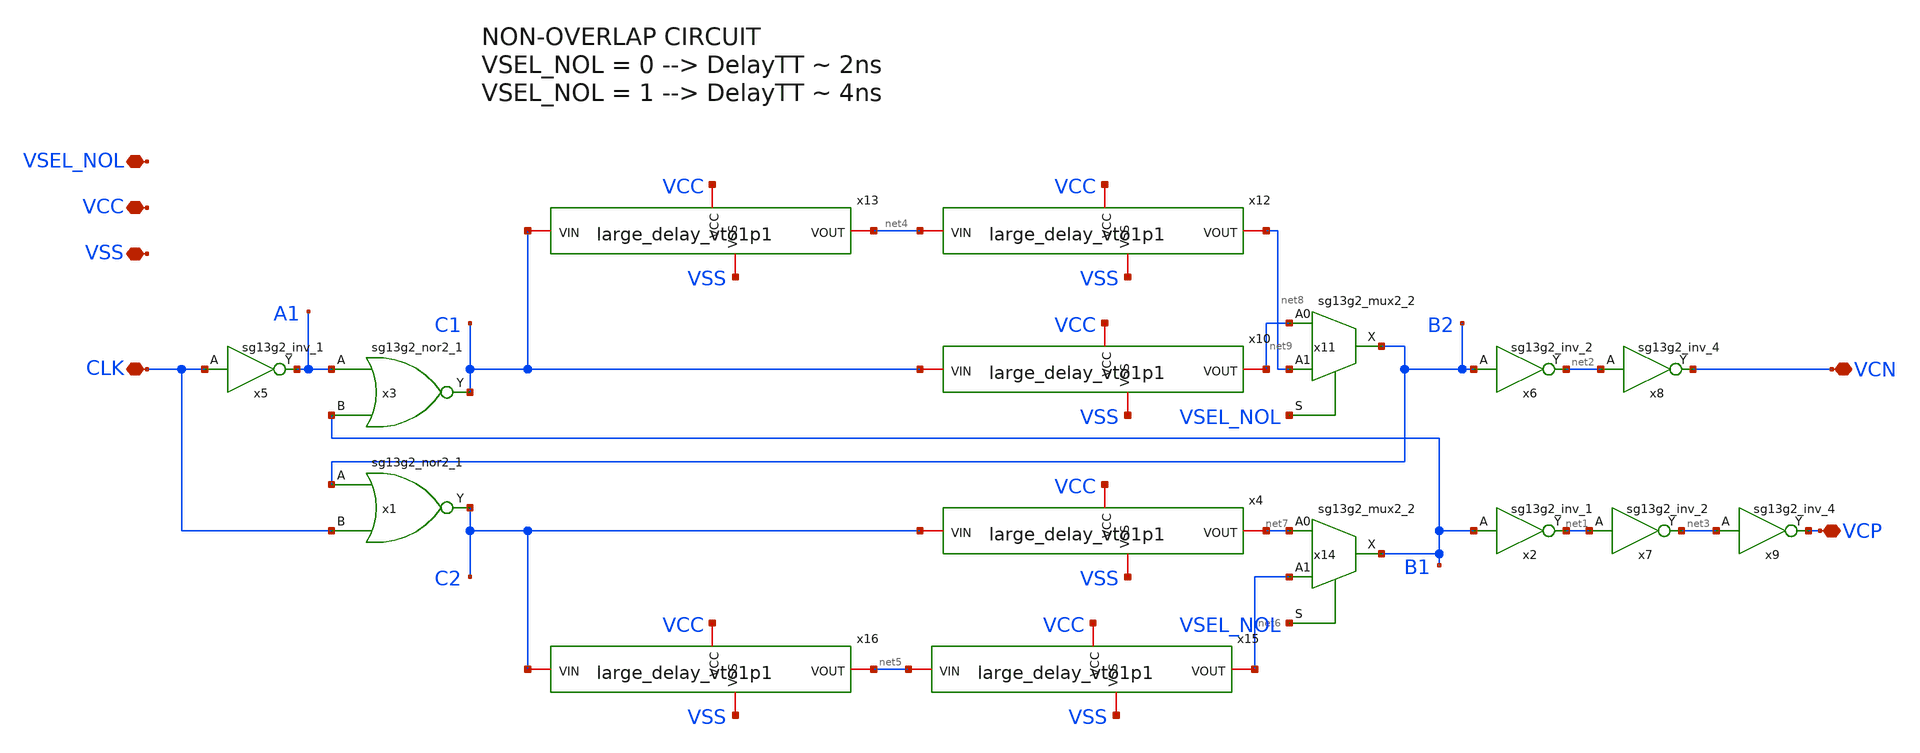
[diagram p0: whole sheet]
** sch_path: AC3E_USM_TDBUCK/design_data/xschem/NOL/NOL2DT_vto1p1.sch
* IHP-GmbH/IHP-Open-PDK/ihp-sg13g2/libs.tech/xschem/sg13g2_stdcells/sg13g2_inv_2.sch:
* Copyright 2023 IHP PDK Authors
* Licensed under the Apache License, Version 2.0 (the "License");
**.subckt NOL2DT_vto1p1 CLK VCP VCN VCC VSS VSEL_NOL
*.iopin CLK
*.iopin VCP
*.iopin VCN
*.iopin VCC
*.iopin VSS
*.iopin VSEL_NOL
x5 A1 CLK VCC VSS sg13g2_inv_1
x3 C1 A1 B1 VCC VSS sg13g2_nor2_1
x1 C2 B2 CLK VCC VSS sg13g2_nor2_1
x2 net1 B1 VCC VSS sg13g2_inv_1
x6 net2 B2 VCC VSS sg13g2_inv_2
x7 net3 net1 VCC VSS sg13g2_inv_2
x8 VCN net2 VCC VSS sg13g2_inv_4
x9 VCP net3 VCC VSS sg13g2_inv_4
x10 VCC VSS C1 net9 large_delay_vto1p1
x4 VCC VSS C2 net7 large_delay_vto1p1
x11 B2 net9 net8 VSEL_NOL VCC VSS sg13g2_mux2_2
x12 VCC VSS net4 net8 large_delay_vto1p1
x13 VCC VSS C1 net4 large_delay_vto1p1
x14 B1 net7 net6 VSEL_NOL VCC VSS sg13g2_mux2_2
x15 VCC VSS net5 net6 large_delay_vto1p1
x16 VCC VSS C2 net5 large_delay_vto1p1
**.ends

* expanding   symbol:  sg13g2_stdcells/sg13g2_inv_1.sym # of pins=2
** sym_path: sg13g2_stdcells/sg13g2_inv_1.sym
** sch_path: sg13g2_stdcells/sg13g2_inv_1.sch
.subckt sg13g2_inv_1 Y A VDD VSS
*.opin Y
*.ipin A
*.iopin VDD
*.iopin VSS
XM1 Y A VSS VSS sg13_lv_nmos w=740.00n l=130.00n ng=1 m=1 mm_ok=1
XM2 Y A VDD VDD sg13_lv_pmos w=1.12u l=130.00n ng=1 m=1 mm_ok=1
.ends


* expanding   symbol:  sg13g2_stdcells/sg13g2_nor2_1.sym # of pins=3
** sym_path: sg13g2_stdcells/sg13g2_nor2_1.sym
** sch_path: sg13g2_stdcells/sg13g2_nor2_1.sch
.subckt sg13g2_nor2_1 Y A B VDD VSS
*.opin Y
*.ipin B
*.ipin A
*.iopin VDD
*.iopin VSS
XM1 Y A VSS VSS sg13_lv_nmos w=740.00n l=130.00n ng=1 m=1 mm_ok=1
XM2 Y B VSS VSS sg13_lv_nmos w=740.00n l=130.00n ng=1 m=1 mm_ok=1
XM3 net1 A VDD VDD sg13_lv_pmos w=1.12u l=130.00n ng=1 m=1 mm_ok=1
XM4 Y B net1 VDD sg13_lv_pmos w=1.12u l=130.00n ng=1 m=1 mm_ok=1
.ends


* expanding   symbol:  sg13g2_stdcells/sg13g2_inv_2.sym # of pins=2
** sym_path: sg13g2_stdcells/sg13g2_inv_2.sym
** sch_path: sg13g2_stdcells/sg13g2_inv_2.sch
.subckt sg13g2_inv_2 Y A VDD VSS
*.opin Y
*.ipin A
*.iopin VDD
*.iopin VSS
XM1 Y A VSS VSS sg13_lv_nmos w=1.48u l=130.00n ng=2 m=1 mm_ok=1
XM2 Y A VDD VDD sg13_lv_pmos w=2.24u l=130.00n ng=2 m=1 mm_ok=1
.ends


* expanding   symbol:  sg13g2_stdcells/sg13g2_inv_4.sym # of pins=2
** sym_path: sg13g2_stdcells/sg13g2_inv_4.sym
** sch_path: sg13g2_stdcells/sg13g2_inv_4.sch
.subckt sg13g2_inv_4 Y A VDD VSS
*.ipin A
*.opin Y
*.iopin VDD
*.iopin VSS
XM1 Y A VSS VSS sg13_lv_nmos w=2.96u l=130.00n ng=4 m=1 mm_ok=1
XM2 Y A VDD VDD sg13_lv_pmos w=4.48u l=130.00n ng=4 m=1 mm_ok=1
.ends


* expanding   symbol:  ../large_delay/large_delay_vto1p1.sym # of pins=4
** sym_path: ../large_delay/large_delay_vto1p1.sym
** sch_path: ../large_delay/large_delay_vto1p1.sch
.subckt large_delay_vto1p1 VCC VSS VIN VOUT
*.iopin VIN
*.iopin VOUT
*.iopin VCC
*.iopin VSS
x1[0] n2 VIN VCC VSS sg13g2_dlygate4sd3_1
x1[1] n3 n2 VCC VSS sg13g2_dlygate4sd3_1
x1[2] n4 n3 VCC VSS sg13g2_dlygate4sd3_1
x1[3] n5 n4 VCC VSS sg13g2_dlygate4sd3_1
x1[4] VOUT n5 VCC VSS sg13g2_dlygate4sd3_1
.ends


* expanding   symbol:  sg13g2_stdcells/sg13g2_mux2_2.sym # of pins=4
** sym_path: sg13g2_stdcells/sg13g2_mux2_2.sym
** sch_path: sg13g2_stdcells/sg13g2_mux2_2.sch
.subckt sg13g2_mux2_2 X A0 A1 S VDD VSS
*.ipin S
*.ipin A0
*.ipin A1
*.opin X
*.iopin VDD
*.iopin VSS
XM1 Sb S VSS VSS sg13_lv_nmos w=550.00n l=130.00n ng=1 m=1 mm_ok=1
XM2 net1 A0 net5 VSS sg13_lv_nmos w=740.00n l=130.00n ng=1 m=1 mm_ok=1
XM3 net5 Sb VSS VSS sg13_lv_nmos w=740.00n l=130.00n ng=1 m=1 mm_ok=1
XM4 net1 A1 net4 VSS sg13_lv_nmos w=740.00n l=130.00n ng=1 m=1 mm_ok=1
XM5 net4 S VSS VSS sg13_lv_nmos w=740.00n l=130.00n ng=1 m=1 mm_ok=1
XM6 X net1 VSS VSS sg13_lv_nmos w=1.48u l=130.00n ng=2 m=1 mm_ok=1
XM7 Sb S VDD VDD sg13_lv_pmos w=840.00n l=130.00n ng=1 m=1 mm_ok=1
XM8 net2 S VDD VDD sg13_lv_pmos w=1.000u l=130.00n ng=1 m=1 mm_ok=1
XM9 net1 A0 net2 VDD sg13_lv_pmos w=1.000u l=130.00n ng=1 m=1 mm_ok=1
XM10 net3 Sb VDD VDD sg13_lv_pmos w=1.000u l=130.00n ng=1 m=1 mm_ok=1
XM11 net1 A1 net3 VDD sg13_lv_pmos w=1.000u l=130.00n ng=1 m=1 mm_ok=1
XM12 X net1 VDD VDD sg13_lv_pmos w=2.24u l=130.00n ng=2 m=1 mm_ok=1
.ends


* expanding   symbol:  sg13g2_stdcells/sg13g2_dlygate4sd3_1.sym # of pins=2
** sym_path: sg13g2_stdcells/sg13g2_dlygate4sd3_1.sym
** sch_path: sg13g2_stdcells/sg13g2_dlygate4sd3_1.sch
.subckt sg13g2_dlygate4sd3_1 X A VDD VSS
*.ipin A
*.opin X
*.iopin VDD
*.iopin VSS
XM1 net3 A VSS VSS sg13_lv_nmos w=420.00n l=130.00n ng=1 m=1 mm_ok=1
XM2 net1 net3 VSS VSS sg13_lv_nmos w=420.00n l=500.0n ng=1 m=1 mm_ok=1
XM3 net2 net1 VSS VSS sg13_lv_nmos w=420.00n l=500.0n ng=1 m=1 mm_ok=1
XM4 X net2 VSS VSS sg13_lv_nmos w=740.00n l=130.00n ng=1 m=1 mm_ok=1
XM5 net3 A VDD VDD sg13_lv_pmos w=420.00n l=130.00n ng=1 m=1 mm_ok=1
XM6 net1 net3 VDD VDD sg13_lv_pmos w=1.000u l=500.0n ng=1 m=1 mm_ok=1
XM7 net2 net1 VDD VDD sg13_lv_pmos w=1.000u l=500.0n ng=1 m=1 mm_ok=1
XM8 X net2 VDD VDD sg13_lv_pmos w=1.12u l=130.00n ng=1 m=1 mm_ok=1
.ends

.end
